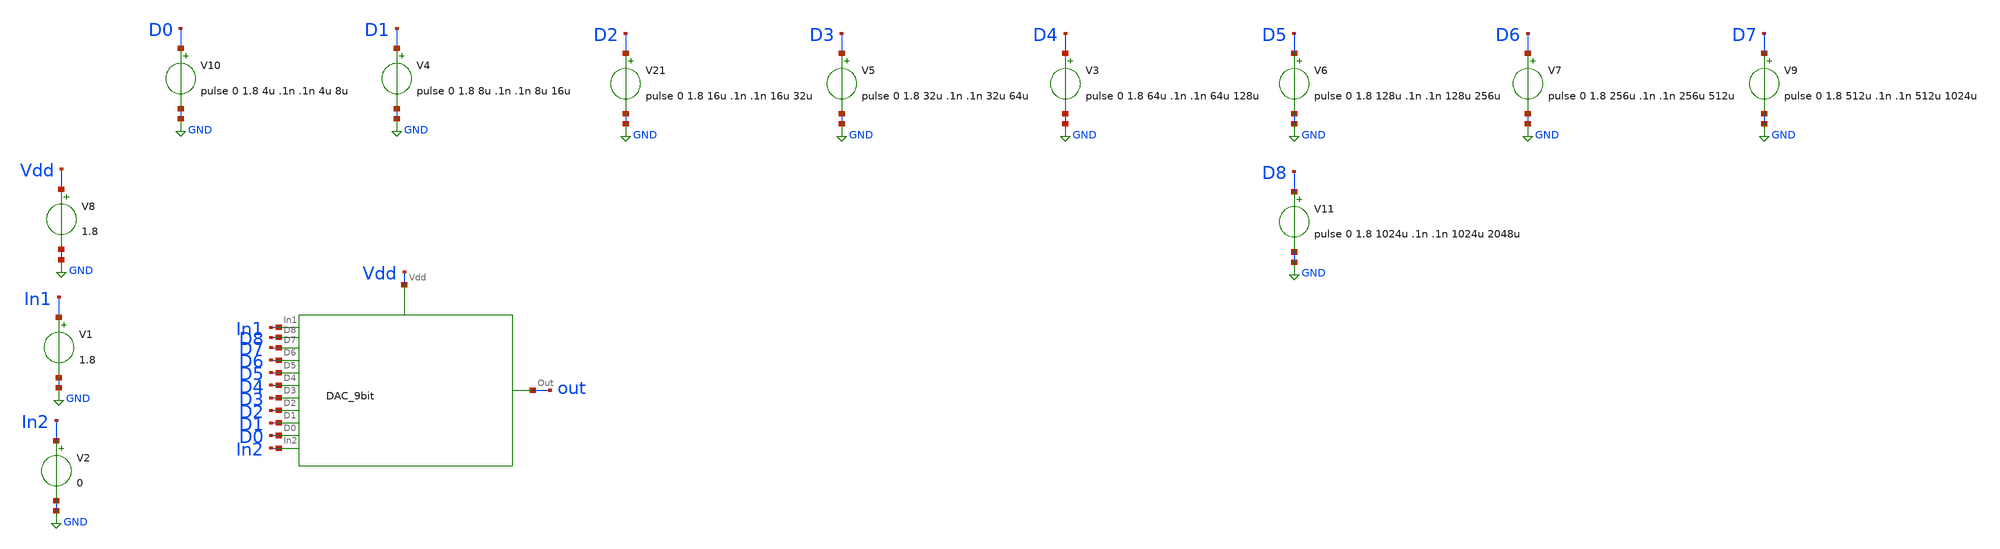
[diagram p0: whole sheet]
** sch_path: DAC/Schematics/DAC_9bit_testbench.sch
**.subckt DAC_9bit_testbench
V8 Vdd GND 1.8
V4 D1 GND pulse 0 1.8 8u .1n .1n 8u 16u
V21 D2 GND pulse 0 1.8 16u .1n .1n 16u 32u
V5 D3 GND pulse 0 1.8 32u .1n .1n 32u 64u
V1 In1 GND 1.8
V2 In2 GND 0
V3 D4 GND pulse 0 1.8 64u .1n .1n 64u 128u
V6 D5 GND pulse 0 1.8 128u .1n .1n 128u 256u
V7 D6 GND pulse 0 1.8 256u .1n .1n 256u 512u
V9 D7 GND pulse 0 1.8 512u .1n .1n 512u 1024u
V10 D0 GND pulse 0 1.8 4u .1n .1n 4u 8u
x1 Vdd out D3 D2 D1 D0 In2 D4 D5 D6 D7 D8 In1 DAC_9bit
V11 D8 GND pulse 0 1.8 1024u .1n .1n 1024u 2048u
**** begin user architecture code

.include $::SKYWATER_MODELS/cells/nfet_01v8/sky130_fd_pr__nfet_01v8__tt.corner.spice
.include $::SKYWATER_MODELS/cells/nfet_01v8_lvt/sky130_fd_pr__nfet_01v8_lvt__tt.corner.spice
.include $::SKYWATER_MODELS/cells/pfet_01v8/sky130_fd_pr__pfet_01v8__tt.corner.spice
.include $::SKYWATER_MODELS/cells/nfet_03v3_nvt/sky130_fd_pr__nfet_03v3_nvt__tt.corner.spice
.include $::SKYWATER_MODELS/cells/nfet_05v0_nvt/sky130_fd_pr__nfet_05v0_nvt__tt.corner.spice
.include $::SKYWATER_MODELS/cells/esd_nfet_01v8/sky130_fd_pr__esd_nfet_01v8__tt.corner.spice
.include $::SKYWATER_MODELS/cells/pfet_01v8_lvt/sky130_fd_pr__pfet_01v8_lvt__tt.corner.spice
.include $::SKYWATER_MODELS/cells/pfet_01v8_hvt/sky130_fd_pr__pfet_01v8_hvt__tt.corner.spice
.include $::SKYWATER_MODELS/cells/esd_pfet_g5v0d10v5/sky130_fd_pr__esd_pfet_g5v0d10v5__tt.corner.spice
.include $::SKYWATER_MODELS/cells/pfet_g5v0d10v5/sky130_fd_pr__pfet_g5v0d10v5__tt.corner.spice
.include $::SKYWATER_MODELS/cells/pfet_g5v0d16v0/sky130_fd_pr__pfet_g5v0d16v0__tt.corner.spice
.include $::SKYWATER_MODELS/cells/nfet_g5v0d10v5/sky130_fd_pr__nfet_g5v0d10v5__tt.corner.spice
.include $::SKYWATER_MODELS/cells/nfet_g5v0d16v0/sky130_fd_pr__nfet_g5v0d16v0__tt_discrete.corner.spice
.include $::SKYWATER_MODELS/cells/esd_nfet_g5v0d10v5/sky130_fd_pr__esd_nfet_g5v0d10v5__tt.corner.spice
.include $::SKYWATER_MODELS/models/corners/tt/nonfet.spice
* Mismatch parameters
.include $::SKYWATER_MODELS/cells/nfet_01v8/sky130_fd_pr__nfet_01v8__mismatch.corner.spice
.include $::SKYWATER_MODELS/cells/pfet_01v8/sky130_fd_pr__pfet_01v8__mismatch.corner.spice
.include $::SKYWATER_MODELS/cells/nfet_01v8_lvt/sky130_fd_pr__nfet_01v8_lvt__mismatch.corner.spice
.include $::SKYWATER_MODELS/cells/pfet_01v8_lvt/sky130_fd_pr__pfet_01v8_lvt__mismatch.corner.spice
.include $::SKYWATER_MODELS/cells/pfet_01v8_hvt/sky130_fd_pr__pfet_01v8_hvt__mismatch.corner.spice
.include $::SKYWATER_MODELS/cells/nfet_g5v0d10v5/sky130_fd_pr__nfet_g5v0d10v5__mismatch.corner.spice
.include $::SKYWATER_MODELS/cells/pfet_g5v0d10v5/sky130_fd_pr__pfet_g5v0d10v5__mismatch.corner.spice
.include $::SKYWATER_MODELS/cells/nfet_05v0_nvt/sky130_fd_pr__nfet_05v0_nvt__mismatch.corner.spice
.include $::SKYWATER_MODELS/cells/nfet_03v3_nvt/sky130_fd_pr__nfet_03v3_nvt__mismatch.corner.spice
* Resistor$::SKYWATER_MODELS/Capacitor
.include $::SKYWATER_MODELS/models/r+c/res_typical__cap_typical.spice
.include $::SKYWATER_MODELS/models/r+c/res_typical__cap_typical__lin.spice
* Special cells
.include $::SKYWATER_MODELS/models/corners/tt/specialized_cells.spice
* All models
.include $::SKYWATER_MODELS/models/all.spice
* Corner
.include $::SKYWATER_MODELS/models/corners/tt/rf.spice
.include ~/skywater-pdk/libraries/sky130_fd_sc_hd/latest/cells/nand3/sky130_fd_sc_hd__nand3_1.spice
.include ~/skywater-pdk/libraries/sky130_fd_sc_hd/latest/cells/nand2/sky130_fd_sc_hd__nand2_1.spice
.include ~/skywater-pdk/libraries/sky130_fd_sc_hd/latest/cells/nor3/sky130_fd_sc_hd__nor3_1.spice
.include ~/skywater-pdk/libraries/sky130_fd_sc_hd/latest/cells/dfrtp/sky130_fd_sc_hd__dfrtp_1.spice
.include ~/skywater-pdk/libraries/sky130_fd_sc_hd/latest/cells/nor2/sky130_fd_sc_hd__nor2_1.spice
.include ~/skywater-pdk/libraries/sky130_fd_sc_hd/latest/cells/dlrbn/sky130_fd_sc_hd__dlrbn_1.spice
.include ~/skywater-pdk/libraries/sky130_fd_sc_hd/latest/cells/a31o/sky130_fd_sc_hd__a31o_2.spice
.include ~/skywater-pdk/libraries/sky130_fd_sc_hd/latest/cells/inv/sky130_fd_sc_hd__inv_1.spice
.include ~/skywater-pdk/libraries/sky130_fd_sc_hd/latest/cells/a222oi/sky130_fd_sc_hd__a222oi_1.spice
.include ~/skywater-pdk/libraries/sky130_fd_sc_hd/latest/cells/or2/sky130_fd_sc_hd__or2_1.spice
.include ~/skywater-pdk/libraries/sky130_fd_sc_hd/latest/cells/o221ai/sky130_fd_sc_hd__o221ai_1.spice


**** end user architecture code
**.ends
.GLOBAL GND
**** begin user architecture code


.temp 25
vvcc vcc 0 1.8
vvss vss 0 0
.control
tran 500u 2048u
plot D0 D1+2 D2+4 D3+6 D4+8 D5+10 D6+12 D7+14 D8+16 out+18
.endc


**** end user architecture code
.end
